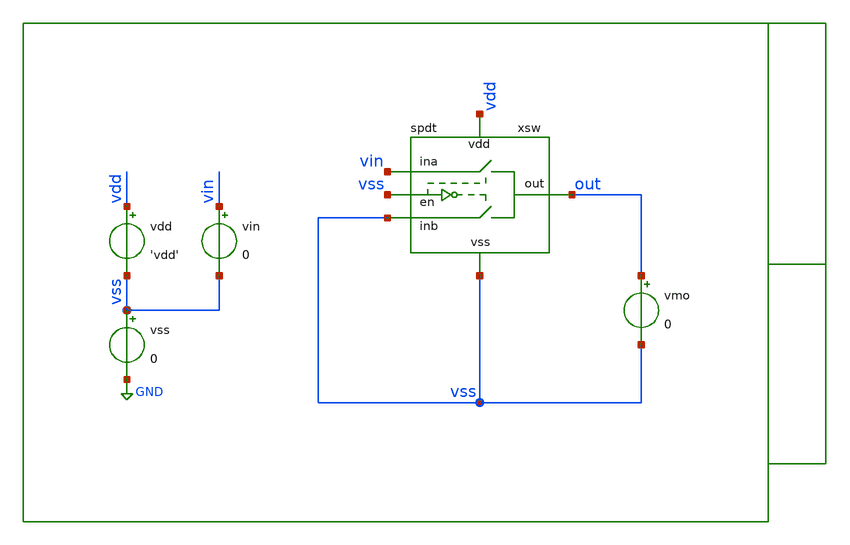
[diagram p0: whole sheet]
** sch_path: xschem/tb/spdt/spdt/dc_spdt_leakage.sch
**.subckt dc_spdt_leakage
vdd vdd vss 'vdd'
vss vss GND 0
xsw out vss vdd vss vss vin spdt
vin vin vss 0
vmo out vss 0
**** begin user architecture code

* Control

.param vdd = 3.3

.temp 27

.save vin#branch
.save vmo#branch

.control
save all

dc vin 0 1.5 0.01

let iin  = abs(vin#branch)
let iout = abs(vmo#branch)

meas dc iin_max max iin
meas dc iout_max max iout

print iin_max
print iout_max

gnuplot p1 iin

set wr_singlescale
set wr_vecnames
wrdata data.csv iin iout

.endc
.end


 * Model Corners

.include $::CORNERS/ngspice/tt.spice
*.include $::CORNERS/ngspice/ff.spice
*.include $::CORNERS/ngspice/ss.spice
*.include $::CORNERS/ngspice/sf.spice
*.include $::CORNERS/ngspice/fs.spice

**** end user architecture code
**.ends

* expanding   symbol:  sch/spdt/spdt/spdt.sym # of pins=6
** sym_path: xschem/sch/spdt/spdt/spdt.sym
** sch_path: xschem/sch/spdt/spdt/spdt.sch
.subckt spdt out en vdd inb vss ina
*.ipin en
*.iopin vss
*.iopin vdd
*.iopin ina
*.iopin out
*.iopin inb
XMI1 enb_buf en vss vss nfet_06v0 L=1u W=4u nf=1 ad='int((nf+1)/2) * W/nf * 0.18u' as='int((nf+2)/2) * W/nf * 0.18u'
+ pd='2*int((nf+1)/2) * (W/nf + 0.18u)' ps='2*int((nf+2)/2) * (W/nf + 0.18u)' nrd='0.18u / W' nrs='0.18u / W'
+ sa=0 sb=0 sd=0 m=1 par=1
XMI2 en_buf enb_buf vss vss nfet_06v0 L=1u W=4u nf=1 ad='int((nf+1)/2) * W/nf * 0.18u' as='int((nf+2)/2) * W/nf * 0.18u'
+ pd='2*int((nf+1)/2) * (W/nf + 0.18u)' ps='2*int((nf+2)/2) * (W/nf + 0.18u)' nrd='0.18u / W' nrs='0.18u / W'
+ sa=0 sb=0 sd=0 m=1 par=1
XMI3 enb_buf en vdd vdd pfet_06v0 L=1u W=8u nf=1 ad='int((nf+1)/2) * W/nf * 0.18u' as='int((nf+2)/2) * W/nf * 0.18u'
+ pd='2*int((nf+1)/2) * (W/nf + 0.18u)' ps='2*int((nf+2)/2) * (W/nf + 0.18u)' nrd='0.18u / W' nrs='0.18u / W'
+ sa=0 sb=0 sd=0 m=1 par=1
XMI4 en_buf enb_buf vdd vdd pfet_06v0 L=1u W=8u nf=1 ad='int((nf+1)/2) * W/nf * 0.18u' as='int((nf+2)/2) * W/nf * 0.18u'
+ pd='2*int((nf+1)/2) * (W/nf + 0.18u)' ps='2*int((nf+2)/2) * (W/nf + 0.18u)' nrd='0.18u / W' nrs='0.18u / W'
+ sa=0 sb=0 sd=0 m=1 par=1
XM2 inb en_buf out vdd pfet_06v0 L=1u W=64u nf=8 ad='int((nf+1)/2) * W/nf * 0.18u' as='int((nf+2)/2) * W/nf * 0.18u'
+ pd='2*int((nf+1)/2) * (W/nf + 0.18u)' ps='2*int((nf+2)/2) * (W/nf + 0.18u)' nrd='0.18u / W' nrs='0.18u / W'
+ sa=0 sb=0 sd=0 m=1 par=1
XM1 inb enb_buf out vss nfet_06v0 L=1u W=32u nf=4 ad='int((nf+1)/2) * W/nf * 0.18u' as='int((nf+2)/2) * W/nf * 0.18u'
+ pd='2*int((nf+1)/2) * (W/nf + 0.18u)' ps='2*int((nf+2)/2) * (W/nf + 0.18u)' nrd='0.18u / W' nrs='0.18u / W'
+ sa=0 sb=0 sd=0 m=1 par=1
XM3 ina en_buf out vss nfet_06v0 L=1u W=32u nf=4 ad='int((nf+1)/2) * W/nf * 0.18u' as='int((nf+2)/2) * W/nf * 0.18u'
+ pd='2*int((nf+1)/2) * (W/nf + 0.18u)' ps='2*int((nf+2)/2) * (W/nf + 0.18u)' nrd='0.18u / W' nrs='0.18u / W'
+ sa=0 sb=0 sd=0 m=1 par=1
XM4 ina enb_buf out vdd pfet_06v0 L=1u W=64u nf=8 ad='int((nf+1)/2) * W/nf * 0.18u' as='int((nf+2)/2) * W/nf * 0.18u'
+ pd='2*int((nf+1)/2) * (W/nf + 0.18u)' ps='2*int((nf+2)/2) * (W/nf + 0.18u)' nrd='0.18u / W' nrs='0.18u / W'
+ sa=0 sb=0 sd=0 m=1 par=1
.ends

.GLOBAL GND
.end
